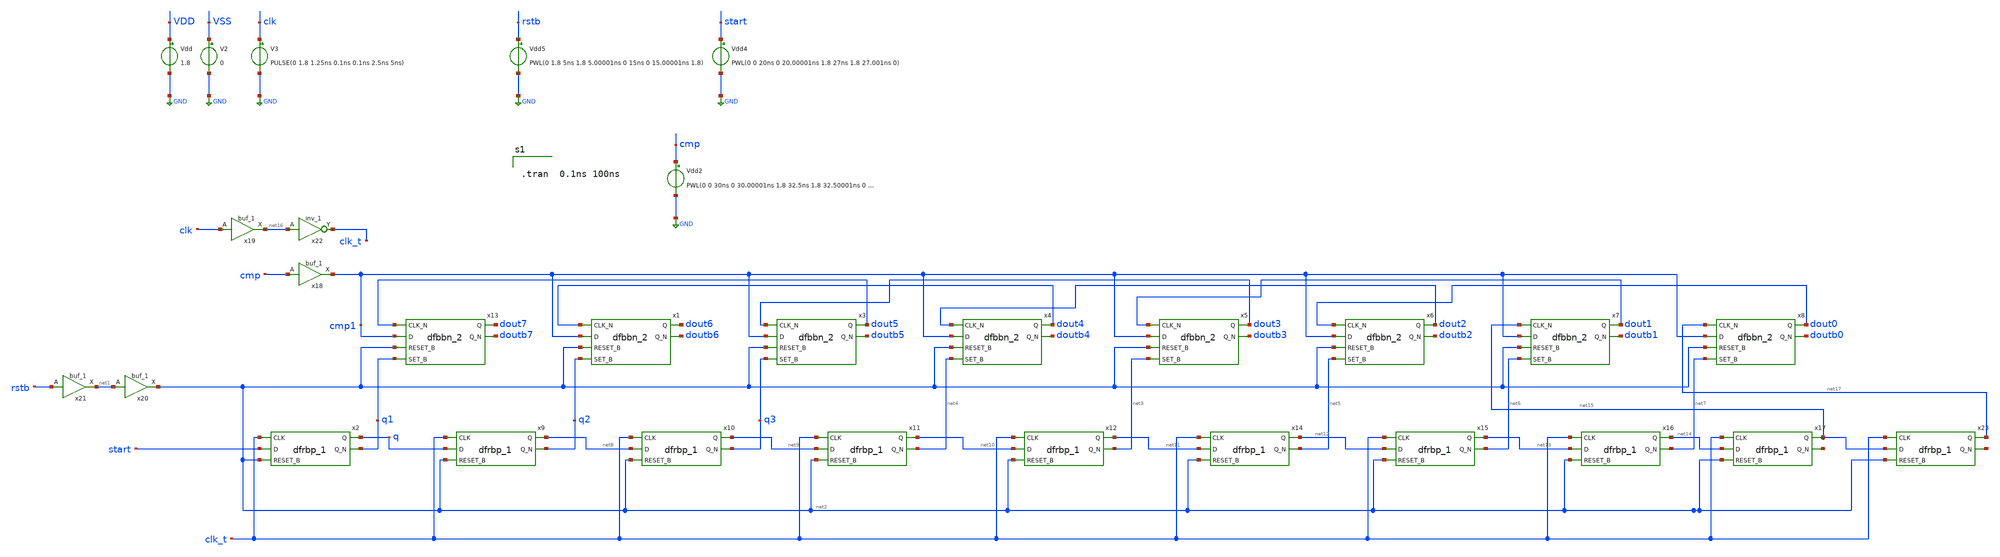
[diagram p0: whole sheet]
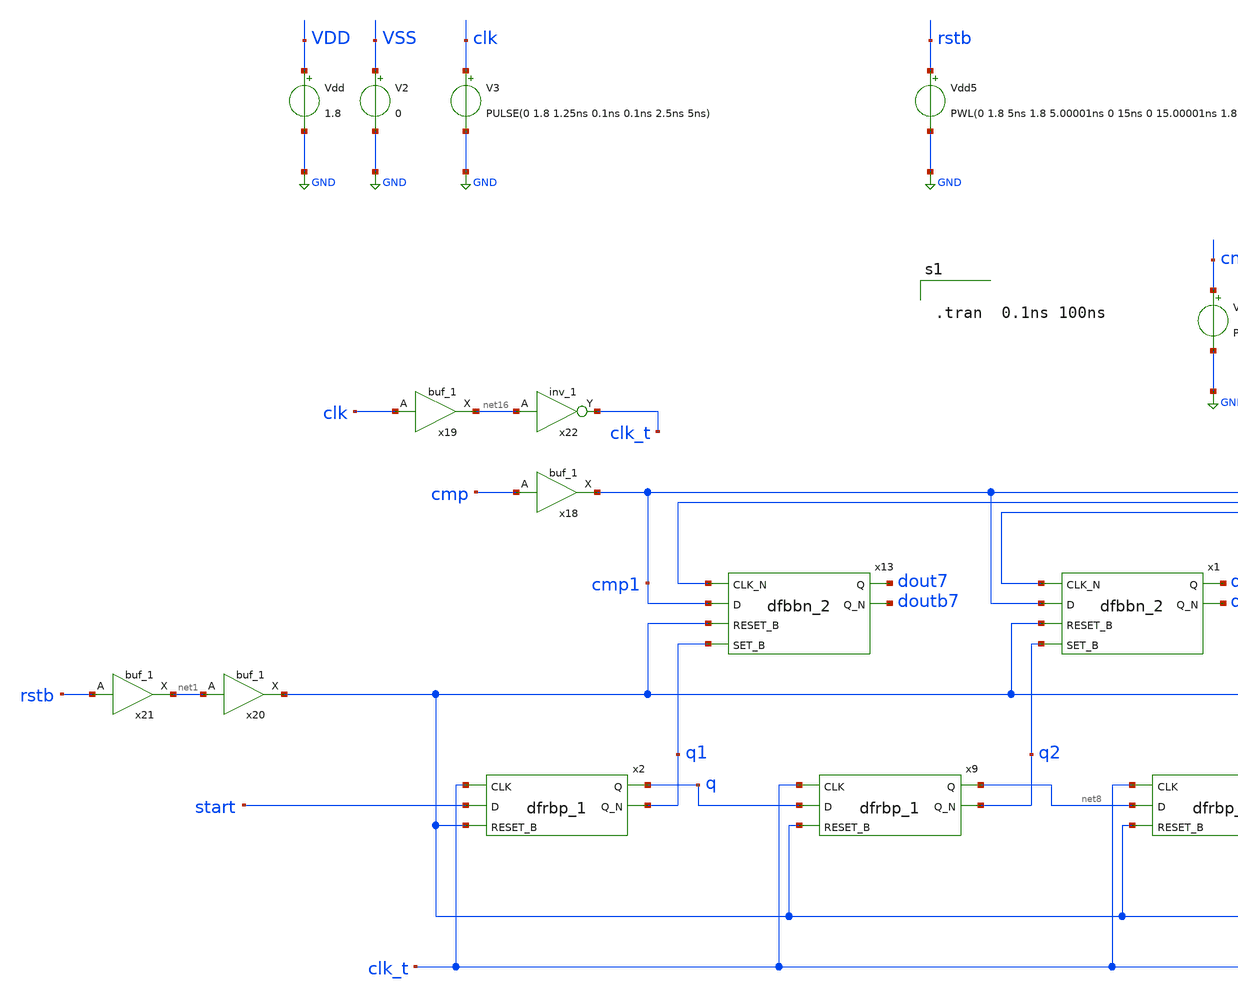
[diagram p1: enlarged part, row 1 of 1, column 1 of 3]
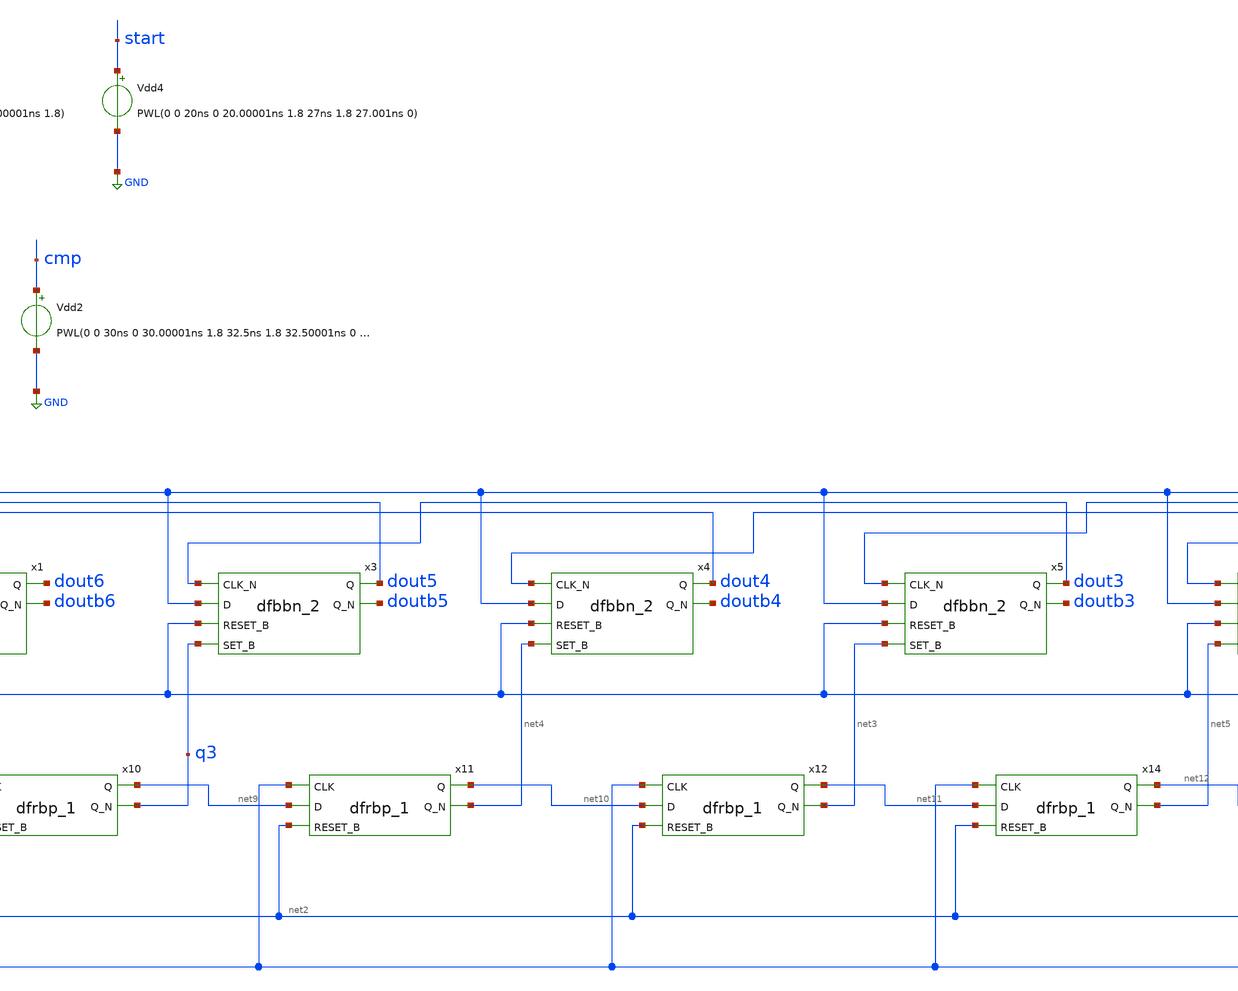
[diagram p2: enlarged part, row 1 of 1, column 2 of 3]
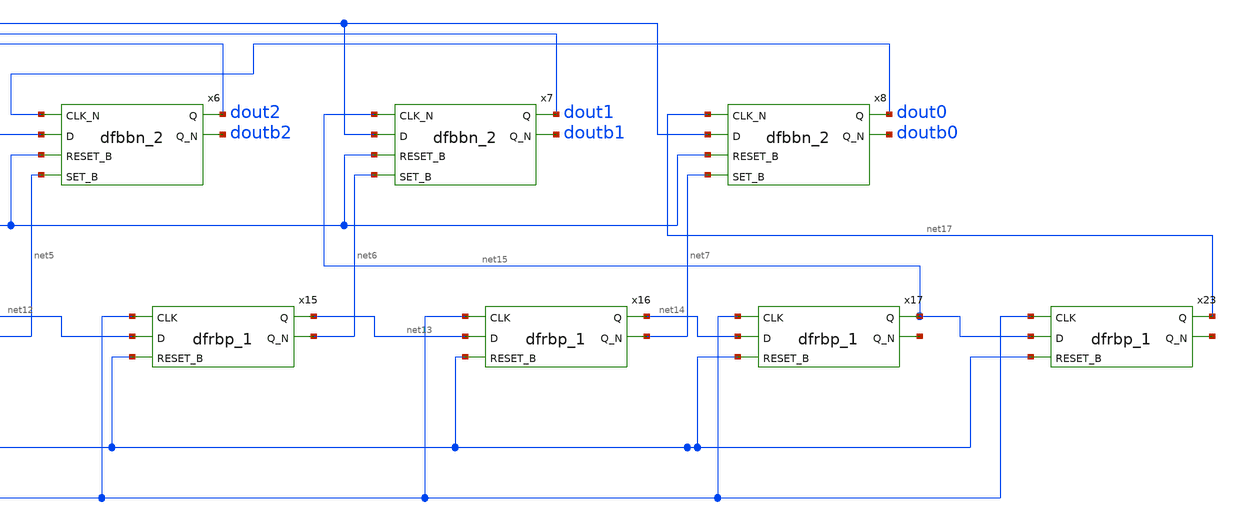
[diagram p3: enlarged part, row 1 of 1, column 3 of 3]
** sch_path: 8bitADC_SARLOGIC_bitdelay.sch
**.subckt 8bitADC_SARLOGIC_bitdelay
x18 cmp VSS VNB VPB VDD cmp1 sky130_fd_sc_hd__buf_1
x19 clk VSS VNB VPB VDD net16 sky130_fd_sc_hd__buf_1
x20 net1 VSS VNB VPB VDD net2 sky130_fd_sc_hd__buf_1
x21 rstb VSS VNB VPB VDD net1 sky130_fd_sc_hd__buf_1
x13 dout5 cmp1 net2 q1 VSS VNB VPB VDD dout7 doutb7 sky130_fd_sc_hd__dfbbn_2
x1 dout4 cmp1 net2 q2 VSS VNB VPB VDD dout6 doutb6 sky130_fd_sc_hd__dfbbn_2
x3 dout3 cmp1 net2 q3 VSS VNB VPB VDD dout5 doutb5 sky130_fd_sc_hd__dfbbn_2
x4 dout2 cmp1 net2 net4 VSS VNB VPB VDD dout4 doutb4 sky130_fd_sc_hd__dfbbn_2
x5 dout1 cmp1 net2 net3 VSS VNB VPB VDD dout3 doutb3 sky130_fd_sc_hd__dfbbn_2
x6 dout0 cmp1 net2 net5 VSS VNB VPB VDD dout2 doutb2 sky130_fd_sc_hd__dfbbn_2
x7 net15 cmp1 net2 net6 VSS VNB VPB VDD dout1 doutb1 sky130_fd_sc_hd__dfbbn_2
x8 net17 cmp1 net2 net7 VSS VNB VPB VDD dout0 doutb0 sky130_fd_sc_hd__dfbbn_2
Vdd VDD GND 1.8
V2 VSS GND 0
Vdd4 start GND PWL(0 0 20ns 0 20.00001ns 1.8 27ns 1.8 27.001ns 0)
Vdd5 rstb GND PWL(0 1.8 5ns 1.8 5.00001ns 0 15ns 0 15.00001ns 1.8)
x2 clk_t start net2 VSS VNB VPB VDD q q1 sky130_fd_sc_hd__dfrbp_1
x9 clk_t q net2 VSS VNB VPB VDD net8 q2 sky130_fd_sc_hd__dfrbp_1
x10 clk_t net8 net2 VSS VNB VPB VDD net9 q3 sky130_fd_sc_hd__dfrbp_1
x11 clk_t net9 net2 VSS VNB VPB VDD net10 net4 sky130_fd_sc_hd__dfrbp_1
x12 clk_t net10 net2 VSS VNB VPB VDD net11 net3 sky130_fd_sc_hd__dfrbp_1
x14 clk_t net11 net2 VSS VNB VPB VDD net12 net5 sky130_fd_sc_hd__dfrbp_1
x15 clk_t net12 net2 VSS VNB VPB VDD net13 net6 sky130_fd_sc_hd__dfrbp_1
x16 clk_t net13 net2 VSS VNB VPB VDD net14 net7 sky130_fd_sc_hd__dfrbp_1
x17 clk_t net14 net2 VSS VNB VPB VDD net15 net18 sky130_fd_sc_hd__dfrbp_1
V3 clk GND PULSE(0 1.8 1.25ns 0.1ns 0.1ns 2.5ns 5ns)
Vdd2 cmp GND PWL(0 0 30ns 0 30.00001ns 1.8 32.5ns 1.8 32.50001ns 0 40ns 0 40.0001ns 1.8 42.5ns 1.8
+ 42.50001ns 0 50ns 0 50.0001ns 1.8 52.5ns 1.8 52.50001ns 0)
x22 net16 VSS VNB VPB VDD clk_t sky130_fd_sc_hd__inv_1
x23 clk_t net15 net2 VSS VNB VPB VDD net17 net19 sky130_fd_sc_hd__dfrbp_1
**** begin user architecture code

** opencircuitdesign pdks install
.lib $::SKYWATER_MODELS/sky130.lib.spice tt
.include $::SKYWATER_STDCELLS/sky130_fd_sc_hd.spice




.tran  0.1ns 100ns




**** end user architecture code
**.ends
.GLOBAL GND
.end
